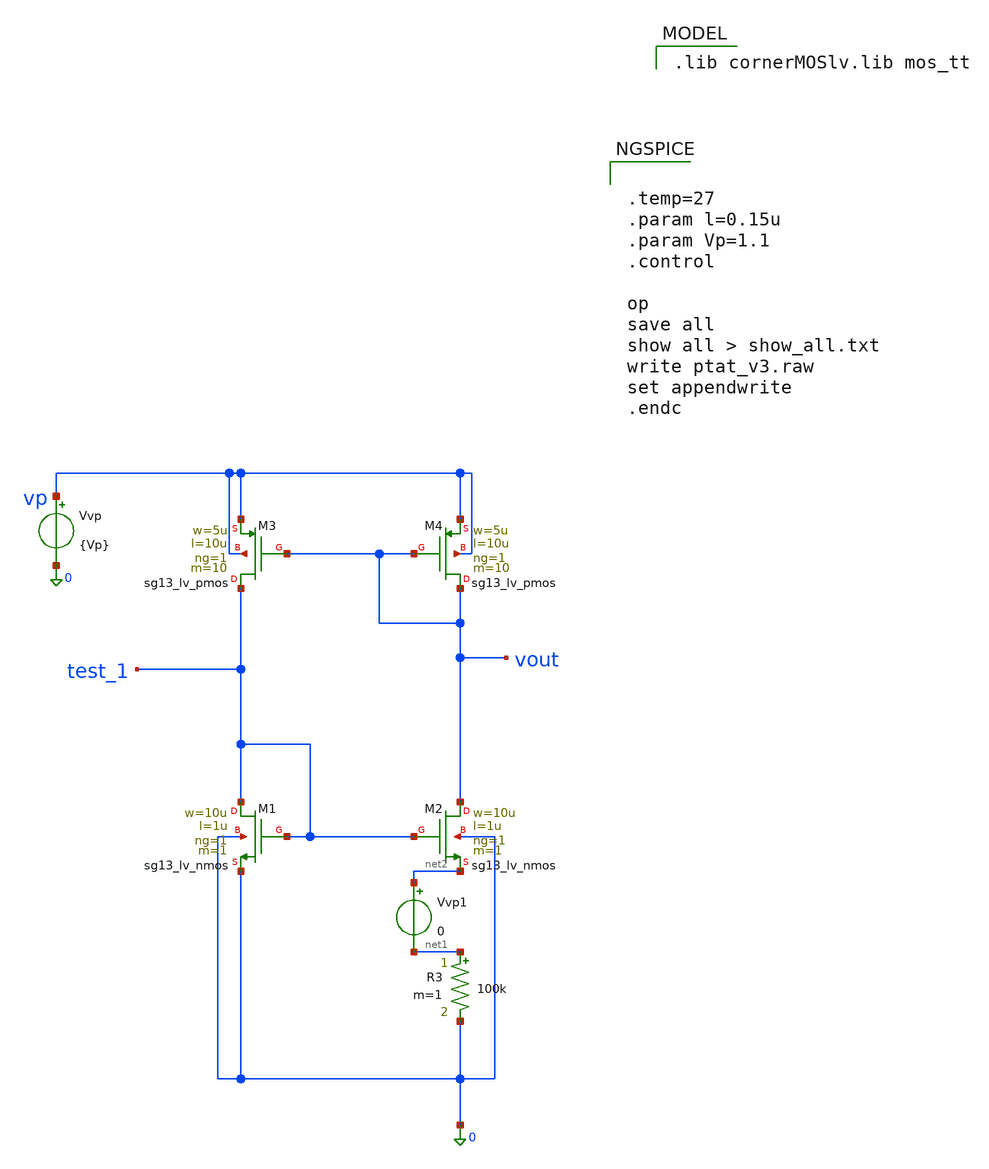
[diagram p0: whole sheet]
** sch_path: schematics/charge_pump/vbias/ptat_v3.sch
**.subckt ptat_v3
XM1 test_1 test_1 0 0 sg13_lv_nmos w=10u l=1u ng=1 m=1 mm_ok=1
XM3 test_1 vout vp vp sg13_lv_pmos w=5u l=10u ng=1 m=10 mm_ok=1
XM2 vout test_1 net2 0 sg13_lv_nmos w=10u l=1u ng=1 m=1 mm_ok=1
XM4 vout vout vp vp sg13_lv_pmos w=5u l=10u ng=1 m=10 mm_ok=1
R3 net1 0 100k m=1
Vvp vp 0 {Vp}
Vvp1 net2 net1 0
.save i(vvp1)
**** begin user architecture code
 .lib cornerMOSlv.lib mos_tt



.temp=27
.param l=0.15u
.param Vp=1.1
.control

op
save all
show all > show_all.txt
write ptat_v3.raw
set appendwrite
.endc


**** end user architecture code
**.ends
.end
